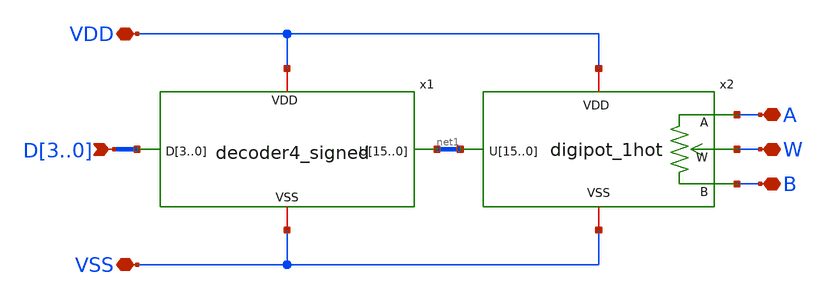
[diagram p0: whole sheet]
** sch_path: xschem/digipot.sch
**.subckt digipot VDD VSS A B W D3,D2,D1,D0
*.iopin VDD
*.iopin VSS
*.iopin A
*.iopin B
*.iopin W
*.ipin D3,D2,D1,D0
x1 VDD D3 D2 D1 D0 net1[15] net1[14] net1[13] net1[12] net1[11] net1[10] net1[9] net1[8] net1[7]
+ net1[6] net1[5] net1[4] net1[3] net1[2] net1[1] net1[0] VSS decoder4_signed
x2 VDD net1[15] net1[14] net1[13] net1[12] net1[11] net1[10] net1[9] net1[8] net1[7] net1[6] net1[5]
+ net1[4] net1[3] net1[2] net1[1] net1[0] A W B VSS digipot_1hot
**.ends

* expanding   symbol:  decoder4_signed.sym # of pins=4
** sym_path: xschem/decoder4_signed.sym
** sch_path: xschem/decoder4_signed.sch
.subckt decoder4_signed VDD D3 D2 D1 D0 U15 U14 U13 U12 U11 U10 U9 U8 U7 U6 U5 U4 U3 U2 U1 U0 VSS
*.iopin VDD
*.iopin VSS
*.opin U15,U14,U13,U12,U11,U10,U9,U8,U7,U6,U5,U4,U3,U2,U1,U0
*.ipin D3,D2,D1,D0
x1 VDD D0 D3 net4 net3 net1 net2 VSS VDD decoder2
x2 VDD D2 D1 U14 U12 U10 U8 VSS net2 decoder2
x3 VDD D2 D1 U6 U4 U2 U0 VSS net1 decoder2
x4 VDD D2 D1 U15 U13 U11 U9 VSS net3 decoder2
x5 VDD D2 D1 U7 U5 U3 U1 VSS net4 decoder2
.ends


* expanding   symbol:  digipot_1hot.sym # of pins=6
** sym_path: xschem/digipot_1hot.sym
** sch_path: xschem/digipot_1hot.sch
.subckt digipot_1hot VDD U15 U14 U13 U12 U11 U10 U9 U8 U7 U6 U5 U4 U3 U2 U1 U0 A W B VSS
*.iopin VDD
*.iopin VSS
*.iopin A
*.iopin B
*.iopin W
*.ipin U15,U14,U13,U12,U11,U10,U9,U8,U7,U6,U5,U4,U3,U2,U1,U0
XR1 A net1 VSS sky130_fd_pr__res_xhigh_po_0p35 L=32 mult=1 m=1
XR2 net1 net2 VSS sky130_fd_pr__res_xhigh_po_0p35 L=32 mult=1 m=1
XR3 net2 net3 VSS sky130_fd_pr__res_xhigh_po_0p35 L=32 mult=1 m=1
XR4 net3 net4 VSS sky130_fd_pr__res_xhigh_po_0p35 L=32 mult=1 m=1
XR5 net4 net5 VSS sky130_fd_pr__res_xhigh_po_0p35 L=32 mult=1 m=1
x1 VDD A W U0 VSS passgate
x2 VDD net1 W U1 VSS passgate
x3 VDD net2 W U2 VSS passgate
x4 VDD net3 W U3 VSS passgate
x5 VDD net4 W U4 VSS passgate
XR6 net5 net6 VSS sky130_fd_pr__res_xhigh_po_0p35 L=32 mult=1 m=1
x6 VDD net5 W U5 VSS passgate
XR7 net6 net7 VSS sky130_fd_pr__res_xhigh_po_0p35 L=32 mult=1 m=1
x7 VDD net6 W U6 VSS passgate
XR8 net8 net7 VSS sky130_fd_pr__res_xhigh_po_0p35 L=32 mult=1 m=1
x8 VDD net7 W U7 VSS passgate
XR9 net8 net9 VSS sky130_fd_pr__res_xhigh_po_0p35 L=32 mult=1 m=1
XR10 net9 net10 VSS sky130_fd_pr__res_xhigh_po_0p35 L=32 mult=1 m=1
XR11 net10 net11 VSS sky130_fd_pr__res_xhigh_po_0p35 L=32 mult=1 m=1
XR12 net11 net12 VSS sky130_fd_pr__res_xhigh_po_0p35 L=32 mult=1 m=1
XR13 net12 net13 VSS sky130_fd_pr__res_xhigh_po_0p35 L=32 mult=1 m=1
x9 VDD net8 W U8 VSS passgate
x10 VDD net9 W U9 VSS passgate
x11 VDD net10 W U10 VSS passgate
x12 VDD net11 W U11 VSS passgate
x13 VDD net12 W U12 VSS passgate
XR14 net13 net14 VSS sky130_fd_pr__res_xhigh_po_0p35 L=32 mult=1 m=1
x14 VDD net13 W U13 VSS passgate
XR15 net14 net15 VSS sky130_fd_pr__res_xhigh_po_0p35 L=32 mult=1 m=1
x15 VDD net14 W U14 VSS passgate
x16 VDD net15 W U15 VSS passgate
XR16 B net15 VSS sky130_fd_pr__res_xhigh_po_0p35 L=32 mult=1 m=1
.ends


* expanding   symbol:  decoder2.sym # of pins=9
** sym_path: xschem/decoder2.sym
** sch_path: xschem/decoder2.sch
.subckt decoder2 VDD D1 D0 U3 U2 U1 U0 VSS EN
*.iopin VDD
*.iopin VSS
*.ipin D0
*.ipin D1
*.opin U0
*.opin U1
*.opin U2
*.opin U3
*.ipin EN
x6 VDD net5 net4 U0 net3 VSS nor3
x7 VDD net5 net1 U1 net3 VSS nor3
x8 VDD net2 net4 U2 net3 VSS nor3
x9 VDD net2 net1 U3 net3 VSS nor3
x1 VDD EN net3 VSS inverter
x2 VDD D0 net1 VSS inverter
x3 VDD net1 net4 VSS inverter
x4 VDD D1 net2 VSS inverter
x5 VDD net2 net5 VSS inverter
.ends


* expanding   symbol:  passgate.sym # of pins=5
** sym_path: xschem/passgate.sym
** sch_path: xschem/passgate.sch
.subckt passgate VDD UA UB EN VSS
*.iopin VSS
*.iopin VDD
*.iopin UA
*.iopin UB
*.ipin EN
XM1 UA EN UB VSS sky130_fd_pr__nfet_g5v0d10v5 L=0.5 W=0.65 nf=1 ad='int((1 + 1)/2) * 0.65 / 1 * 0.29'
+ as='int((1 + 2)/2) * 0.65 / 1 * 0.29' pd='2*int((1 + 1)/2) * (0.65 / 1 + 0.29)' ps='2*int((1 + 2)/2) * (0.65 / 1 + 0.29)'
+ nrd='0.29 / 0.65 ' nrs='0.29 / 0.65 ' sa=0 sb=0 sd=0 mult=1 m=1
XM2 UA net1 UB VDD sky130_fd_pr__pfet_g5v0d10v5 L=0.5 W=1 nf=1 ad='int((1 + 1)/2) * 1 / 1 * 0.29' as='int((1 + 2)/2) * 1 / 1 * 0.29'
+ pd='2*int((1 + 1)/2) * (1 / 1 + 0.29)' ps='2*int((1 + 2)/2) * (1 / 1 + 0.29)' nrd='0.29 / 1 ' nrs='0.29 / 1 '
+ sa=0 sb=0 sd=0 mult=1 m=1
x1 VDD EN net1 VSS inverter
.ends


* expanding   symbol:  nor3.sym # of pins=6
** sym_path: xschem/nor3.sym
** sch_path: xschem/nor3.sch
.subckt nor3 VDD A B OUT C VSS
*.iopin VSS
*.iopin VDD
*.ipin B
*.ipin A
*.ipin C
*.opin OUT
XM2 OUT B VSS VSS sky130_fd_pr__nfet_g5v0d10v5 L=0.5 W=0.65 nf=1 ad='int((1 + 1)/2) * 0.65 / 1 * 0.29'
+ as='int((1 + 2)/2) * 0.65 / 1 * 0.29' pd='2*int((1 + 1)/2) * (0.65 / 1 + 0.29)' ps='2*int((1 + 2)/2) * (0.65 / 1 + 0.29)'
+ nrd='0.29 / 0.65 ' nrs='0.29 / 0.65 ' sa=0 sb=0 sd=0 mult=1 m=1
XM1 OUT A VSS VSS sky130_fd_pr__nfet_g5v0d10v5 L=0.5 W=0.65 nf=1 ad='int((1 + 1)/2) * 0.65 / 1 * 0.29'
+ as='int((1 + 2)/2) * 0.65 / 1 * 0.29' pd='2*int((1 + 1)/2) * (0.65 / 1 + 0.29)' ps='2*int((1 + 2)/2) * (0.65 / 1 + 0.29)'
+ nrd='0.29 / 0.65 ' nrs='0.29 / 0.65 ' sa=0 sb=0 sd=0 mult=1 m=1
XM4 net1 A VDD VDD sky130_fd_pr__pfet_g5v0d10v5 L=0.5 W=1 nf=1 ad='int((1 + 1)/2) * 1 / 1 * 0.29' as='int((1 + 2)/2) * 1 / 1 * 0.29'
+ pd='2*int((1 + 1)/2) * (1 / 1 + 0.29)' ps='2*int((1 + 2)/2) * (1 / 1 + 0.29)' nrd='0.29 / 1 ' nrs='0.29 / 1 '
+ sa=0 sb=0 sd=0 mult=1 m=1
XM3 OUT C VSS VSS sky130_fd_pr__nfet_g5v0d10v5 L=0.5 W=0.65 nf=1 ad='int((1 + 1)/2) * 0.65 / 1 * 0.29'
+ as='int((1 + 2)/2) * 0.65 / 1 * 0.29' pd='2*int((1 + 1)/2) * (0.65 / 1 + 0.29)' ps='2*int((1 + 2)/2) * (0.65 / 1 + 0.29)'
+ nrd='0.29 / 0.65 ' nrs='0.29 / 0.65 ' sa=0 sb=0 sd=0 mult=1 m=1
XM5 net2 B net1 VDD sky130_fd_pr__pfet_g5v0d10v5 L=0.5 W=1 nf=1 ad='int((1 + 1)/2) * 1 / 1 * 0.29' as='int((1 + 2)/2) * 1 / 1 * 0.29'
+ pd='2*int((1 + 1)/2) * (1 / 1 + 0.29)' ps='2*int((1 + 2)/2) * (1 / 1 + 0.29)' nrd='0.29 / 1 ' nrs='0.29 / 1 '
+ sa=0 sb=0 sd=0 mult=1 m=1
XM6 OUT C net2 VDD sky130_fd_pr__pfet_g5v0d10v5 L=0.5 W=1 nf=1 ad='int((1 + 1)/2) * 1 / 1 * 0.29' as='int((1 + 2)/2) * 1 / 1 * 0.29'
+ pd='2*int((1 + 1)/2) * (1 / 1 + 0.29)' ps='2*int((1 + 2)/2) * (1 / 1 + 0.29)' nrd='0.29 / 1 ' nrs='0.29 / 1 '
+ sa=0 sb=0 sd=0 mult=1 m=1
.ends


* expanding   symbol:  inverter.sym # of pins=4
** sym_path: xschem/inverter.sym
** sch_path: xschem/inverter.sch
.subckt inverter VDD IN OUT VSS
*.iopin VSS
*.iopin VDD
*.ipin IN
*.opin OUT
XM1 OUT IN VSS VSS sky130_fd_pr__nfet_g5v0d10v5 L=0.5 W=0.65 nf=1 ad='int((1 + 1)/2) * 0.65 / 1 * 0.29'
+ as='int((1 + 2)/2) * 0.65 / 1 * 0.29' pd='2*int((1 + 1)/2) * (0.65 / 1 + 0.29)' ps='2*int((1 + 2)/2) * (0.65 / 1 + 0.29)'
+ nrd='0.29 / 0.65 ' nrs='0.29 / 0.65 ' sa=0 sb=0 sd=0 mult=1 m=1
XM2 OUT IN VDD VDD sky130_fd_pr__pfet_g5v0d10v5 L=0.5 W=1 nf=1 ad='int((1 + 1)/2) * 1 / 1 * 0.29' as='int((1 + 2)/2) * 1 / 1 * 0.29'
+ pd='2*int((1 + 1)/2) * (1 / 1 + 0.29)' ps='2*int((1 + 2)/2) * (1 / 1 + 0.29)' nrd='0.29 / 1 ' nrs='0.29 / 1 '
+ sa=0 sb=0 sd=0 mult=1 m=1
.ends

.end
